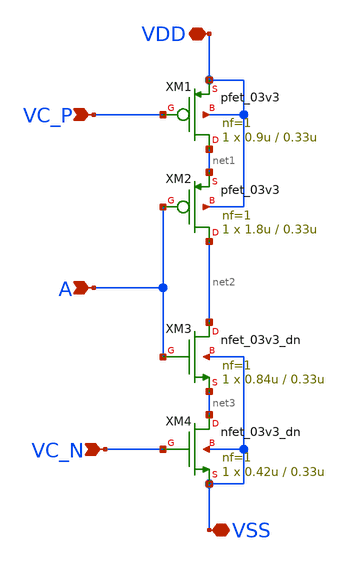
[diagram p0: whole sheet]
** sch_path: vco_inverter_end.sch
**.subckt vco_inverter_end VDD VSS A VC_N VC_P
*.iopin VDD
*.iopin VSS
*.ipin A
*.ipin VC_N
*.ipin VC_P
XM1 net1 VC_P VDD VDD pfet_03v3 L=0.33u W=0.9u nf=1 ad='int((nf+1)/2) * W/nf * 0.18u' as='int((nf+2)/2) * W/nf * 0.18u'
+ pd='2*int((nf+1)/2) * (W/nf + 0.18u)' ps='2*int((nf+2)/2) * (W/nf + 0.18u)' nrd='0.18u / W' nrs='0.18u / W'
+ sa=0 sb=0 sd=0 m=1
XM2 net2 A net1 VDD pfet_03v3 L=0.33u W=1.8u nf=1 ad='int((nf+1)/2) * W/nf * 0.18u' as='int((nf+2)/2) * W/nf * 0.18u'
+ pd='2*int((nf+1)/2) * (W/nf + 0.18u)' ps='2*int((nf+2)/2) * (W/nf + 0.18u)' nrd='0.18u / W' nrs='0.18u / W'
+ sa=0 sb=0 sd=0 m=1
XM3 net2 A net3 VSS nfet_03v3_dn L=0.33u W=0.84u nf=1 ad='int((nf+1)/2) * W/nf * 0.18u' as='int((nf+2)/2) * W/nf * 0.18u'
+ pd='2*int((nf+1)/2) * (W/nf + 0.18u)' ps='2*int((nf+2)/2) * (W/nf + 0.18u)' nrd='0.18u / W' nrs='0.18u / W'
+ sa=0 sb=0 sd=0 m=1
XM4 net3 VC_N VSS VSS nfet_03v3_dn L=0.33u W=0.42u nf=1 ad='int((nf+1)/2) * W/nf * 0.18u' as='int((nf+2)/2) * W/nf * 0.18u'
+ pd='2*int((nf+1)/2) * (W/nf + 0.18u)' ps='2*int((nf+2)/2) * (W/nf + 0.18u)' nrd='0.18u / W' nrs='0.18u / W'
+ sa=0 sb=0 sd=0 m=1
**.ends
.end
